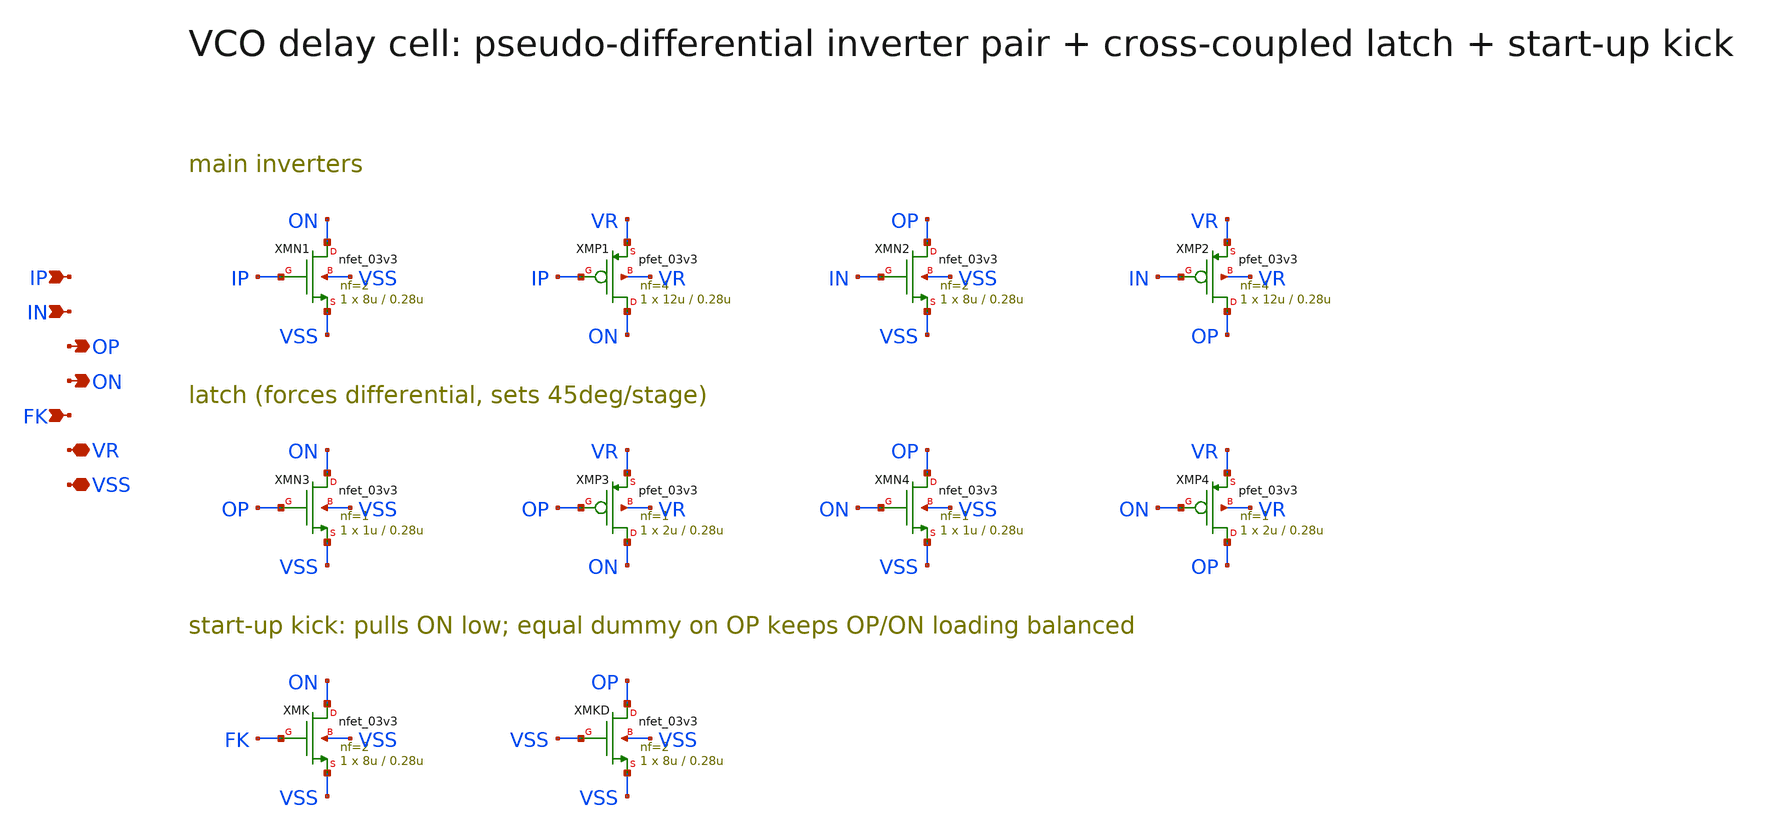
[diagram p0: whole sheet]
** sch_path: v1_claude/archive/legacy_cells/xschem/vco_cellk.sch
**.subckt vco_cellk IP IN OP ON FK VR VSS
*.ipin IP
*.ipin IN
*.opin OP
*.opin ON
*.ipin FK
*.iopin VR
*.iopin VSS
XMN1 ON IP VSS VSS nfet_03v3 L=0.28u W=8u nf=2 ad='int((nf+1)/2) * W/nf * 0.18u' as='int((nf+2)/2) * W/nf * 0.18u'
+ pd='2*int((nf+1)/2) * (W/nf + 0.18u)' ps='2*int((nf+2)/2) * (W/nf + 0.18u)' nrd='0.18u / W' nrs='0.18u / W'
+ sa=0 sb=0 sd=0 m=1
XMP1 ON IP VR VR pfet_03v3 L=0.28u W=12u nf=4 ad='int((nf+1)/2) * W/nf * 0.18u' as='int((nf+2)/2) * W/nf * 0.18u'
+ pd='2*int((nf+1)/2) * (W/nf + 0.18u)' ps='2*int((nf+2)/2) * (W/nf + 0.18u)' nrd='0.18u / W' nrs='0.18u / W'
+ sa=0 sb=0 sd=0 m=1
XMN2 OP IN VSS VSS nfet_03v3 L=0.28u W=8u nf=2 ad='int((nf+1)/2) * W/nf * 0.18u' as='int((nf+2)/2) * W/nf * 0.18u'
+ pd='2*int((nf+1)/2) * (W/nf + 0.18u)' ps='2*int((nf+2)/2) * (W/nf + 0.18u)' nrd='0.18u / W' nrs='0.18u / W'
+ sa=0 sb=0 sd=0 m=1
XMP2 OP IN VR VR pfet_03v3 L=0.28u W=12u nf=4 ad='int((nf+1)/2) * W/nf * 0.18u' as='int((nf+2)/2) * W/nf * 0.18u'
+ pd='2*int((nf+1)/2) * (W/nf + 0.18u)' ps='2*int((nf+2)/2) * (W/nf + 0.18u)' nrd='0.18u / W' nrs='0.18u / W'
+ sa=0 sb=0 sd=0 m=1
XMN3 ON OP VSS VSS nfet_03v3 L=0.28u W=1u nf=1 ad='int((nf+1)/2) * W/nf * 0.18u' as='int((nf+2)/2) * W/nf * 0.18u'
+ pd='2*int((nf+1)/2) * (W/nf + 0.18u)' ps='2*int((nf+2)/2) * (W/nf + 0.18u)' nrd='0.18u / W' nrs='0.18u / W'
+ sa=0 sb=0 sd=0 m=1
XMP3 ON OP VR VR pfet_03v3 L=0.28u W=2u nf=1 ad='int((nf+1)/2) * W/nf * 0.18u' as='int((nf+2)/2) * W/nf * 0.18u'
+ pd='2*int((nf+1)/2) * (W/nf + 0.18u)' ps='2*int((nf+2)/2) * (W/nf + 0.18u)' nrd='0.18u / W' nrs='0.18u / W'
+ sa=0 sb=0 sd=0 m=1
XMN4 OP ON VSS VSS nfet_03v3 L=0.28u W=1u nf=1 ad='int((nf+1)/2) * W/nf * 0.18u' as='int((nf+2)/2) * W/nf * 0.18u'
+ pd='2*int((nf+1)/2) * (W/nf + 0.18u)' ps='2*int((nf+2)/2) * (W/nf + 0.18u)' nrd='0.18u / W' nrs='0.18u / W'
+ sa=0 sb=0 sd=0 m=1
XMP4 OP ON VR VR pfet_03v3 L=0.28u W=2u nf=1 ad='int((nf+1)/2) * W/nf * 0.18u' as='int((nf+2)/2) * W/nf * 0.18u'
+ pd='2*int((nf+1)/2) * (W/nf + 0.18u)' ps='2*int((nf+2)/2) * (W/nf + 0.18u)' nrd='0.18u / W' nrs='0.18u / W'
+ sa=0 sb=0 sd=0 m=1
XMK ON FK VSS VSS nfet_03v3 L=0.28u W=8u nf=2 ad='int((nf+1)/2) * W/nf * 0.18u' as='int((nf+2)/2) * W/nf * 0.18u'
+ pd='2*int((nf+1)/2) * (W/nf + 0.18u)' ps='2*int((nf+2)/2) * (W/nf + 0.18u)' nrd='0.18u / W' nrs='0.18u / W'
+ sa=0 sb=0 sd=0 m=1
XMKD OP VSS VSS VSS nfet_03v3 L=0.28u W=8u nf=2 ad='int((nf+1)/2) * W/nf * 0.18u' as='int((nf+2)/2) * W/nf * 0.18u'
+ pd='2*int((nf+1)/2) * (W/nf + 0.18u)' ps='2*int((nf+2)/2) * (W/nf + 0.18u)' nrd='0.18u / W' nrs='0.18u / W'
+ sa=0 sb=0 sd=0 m=1
**.ends
.end
